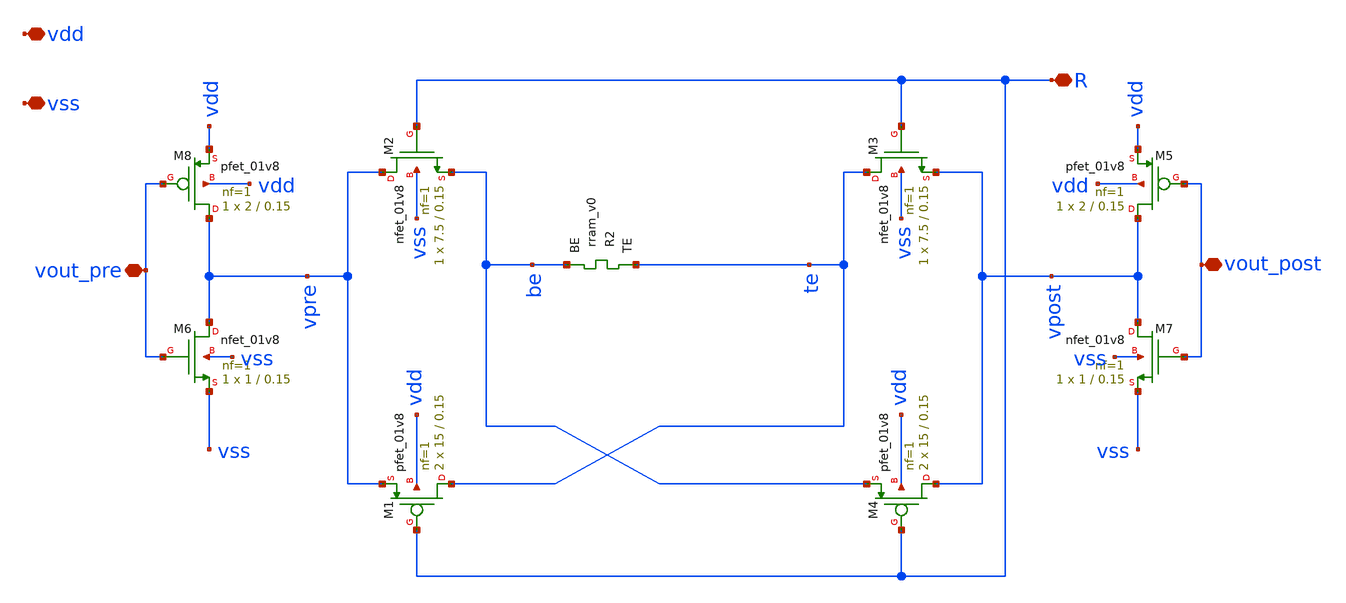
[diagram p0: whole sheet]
** sch_path: Synapse/rstdp_switched.sch
**.subckt rstdp_switched vdd vss R vout_post vout_pre
*.iopin vdd
*.iopin vss
*.iopin R
*.iopin vout_post
*.iopin vout_pre
XR2 te be rram_v0
XM2 vpre R be vss sky130_fd_pr__nfet_01v8 L=0.15 W=7.5 nf=1 ad='int((nf+1)/2) * W/nf * 0.29' as='int((nf+2)/2) * W/nf * 0.29'
+ pd='2*int((nf+1)/2) * (W/nf + 0.29)' ps='2*int((nf+2)/2) * (W/nf + 0.29)' nrd='0.29 / W' nrs='0.29 / W'
+ sa=0 sb=0 sd=0 mult=1 m=1
XM3 te R vpost vss sky130_fd_pr__nfet_01v8 L=0.15 W=7.5 nf=1 ad='int((nf+1)/2) * W/nf * 0.29' as='int((nf+2)/2) * W/nf * 0.29'
+ pd='2*int((nf+1)/2) * (W/nf + 0.29)' ps='2*int((nf+2)/2) * (W/nf + 0.29)' nrd='0.29 / W' nrs='0.29 / W'
+ sa=0 sb=0 sd=0 mult=1 m=1
XM1 te R vpre vdd sky130_fd_pr__pfet_01v8 L=0.15 W=15 nf=1 ad='int((nf+1)/2) * W/nf * 0.29' as='int((nf+2)/2) * W/nf * 0.29'
+ pd='2*int((nf+1)/2) * (W/nf + 0.29)' ps='2*int((nf+2)/2) * (W/nf + 0.29)' nrd='0.29 / W' nrs='0.29 / W'
+ sa=0 sb=0 sd=0 mult=2 m=2
XM4 vpost R be vdd sky130_fd_pr__pfet_01v8 L=0.15 W=15 nf=1 ad='int((nf+1)/2) * W/nf * 0.29' as='int((nf+2)/2) * W/nf * 0.29'
+ pd='2*int((nf+1)/2) * (W/nf + 0.29)' ps='2*int((nf+2)/2) * (W/nf + 0.29)' nrd='0.29 / W' nrs='0.29 / W'
+ sa=0 sb=0 sd=0 mult=2 m=2
XM7 vpost vout_post vss vss sky130_fd_pr__nfet_01v8 L=0.15 W=1 nf=1 ad='int((1 + 1)/2) * 1 / 1 * 0.29'
+ as='int((1 + 2)/2) * 1 / 1 * 0.29' pd='2*int((1 + 1)/2) * (1 / 1 + 0.29)' ps='2*int((1 + 2)/2) * (1 / 1 + 0.29)'
+ nrd='0.29 / 1 ' nrs='0.29 / 1 ' sa=0 sb=0 sd=0 mult=1 m=1
XM5 vpost vout_post vdd vdd sky130_fd_pr__pfet_01v8 L=0.15 W=2 nf=1 ad='int((nf+1)/2) * W/nf * 0.29'
+ as='int((nf+2)/2) * W/nf * 0.29' pd='2*int((nf+1)/2) * (W/nf + 0.29)' ps='2*int((nf+2)/2) * (W/nf + 0.29)'
+ nrd='0.29 / W' nrs='0.29 / W' sa=0 sb=0 sd=0 mult=1 m=1
XM6 vpre vout_pre vss vss sky130_fd_pr__nfet_01v8 L=0.15 W=1 nf=1 ad='int((1 + 1)/2) * 1 / 1 * 0.29'
+ as='int((1 + 2)/2) * 1 / 1 * 0.29' pd='2*int((1 + 1)/2) * (1 / 1 + 0.29)' ps='2*int((1 + 2)/2) * (1 / 1 + 0.29)'
+ nrd='0.29 / 1 ' nrs='0.29 / 1 ' sa=0 sb=0 sd=0 mult=1 m=1
XM8 vpre vout_pre vdd vdd sky130_fd_pr__pfet_01v8 L=0.15 W=2 nf=1 ad='int((nf+1)/2) * W/nf * 0.29' as='int((nf+2)/2) * W/nf * 0.29'
+ pd='2*int((nf+1)/2) * (W/nf + 0.29)' ps='2*int((nf+2)/2) * (W/nf + 0.29)' nrd='0.29 / W' nrs='0.29 / W'
+ sa=0 sb=0 sd=0 mult=1 m=1
**.ends
.end
